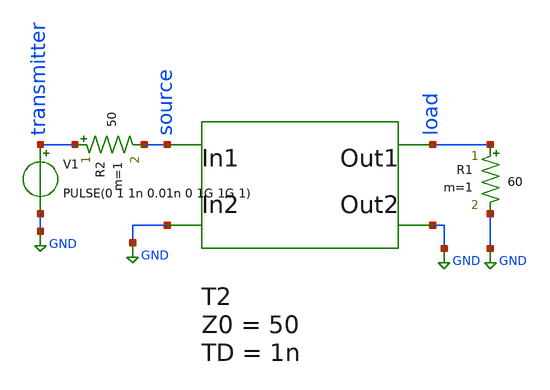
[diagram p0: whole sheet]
** sch_path: tline/tline_tb.sch
**.subckt tline_tb
V1 transmitter GND PULSE(0 1 1n 0.01n 0 1G 1G 1)
R1 load GND 60 m=1
R2 transmitter source 50 m=1
T2 source GND load GND Z0=50 TD=1n
**** begin user architecture code



.tran 0.001n 50n
.save all
.control
run
write tline_tb.raw
plot v(source) v(load) v(transmitter)
endc



**** end user architecture code
**.ends
.GLOBAL GND
.end
